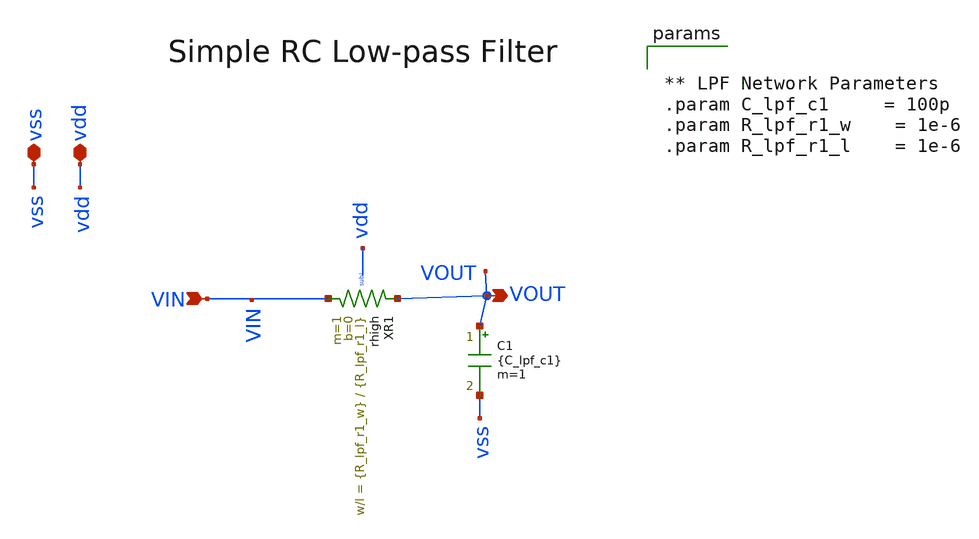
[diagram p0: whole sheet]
** sch_path: analog-db/drawings/ldo-005-ti-ldo-buffer-ref/ihp130/lpf/lpf_rc.sch
**.subckt lpf_rc VIN vdd vss VOUT
*.ipin VIN
*.iopin vdd
*.iopin vss
*.opin VOUT
XR1 VIN VOUT sub! rhigh w={R_lpf_r1_w} l={R_lpf_r1_l} m=1 b=0
C1 VOUT vss {C_lpf_c1} m=1
**** begin user architecture code

** LPF Network Parameters
.param C_lpf_c1 	= 100p
.param R_lpf_r1_w	= 1e-6
.param R_lpf_r1_l	= 1e-6


**** end user architecture code
**.ends
.end
